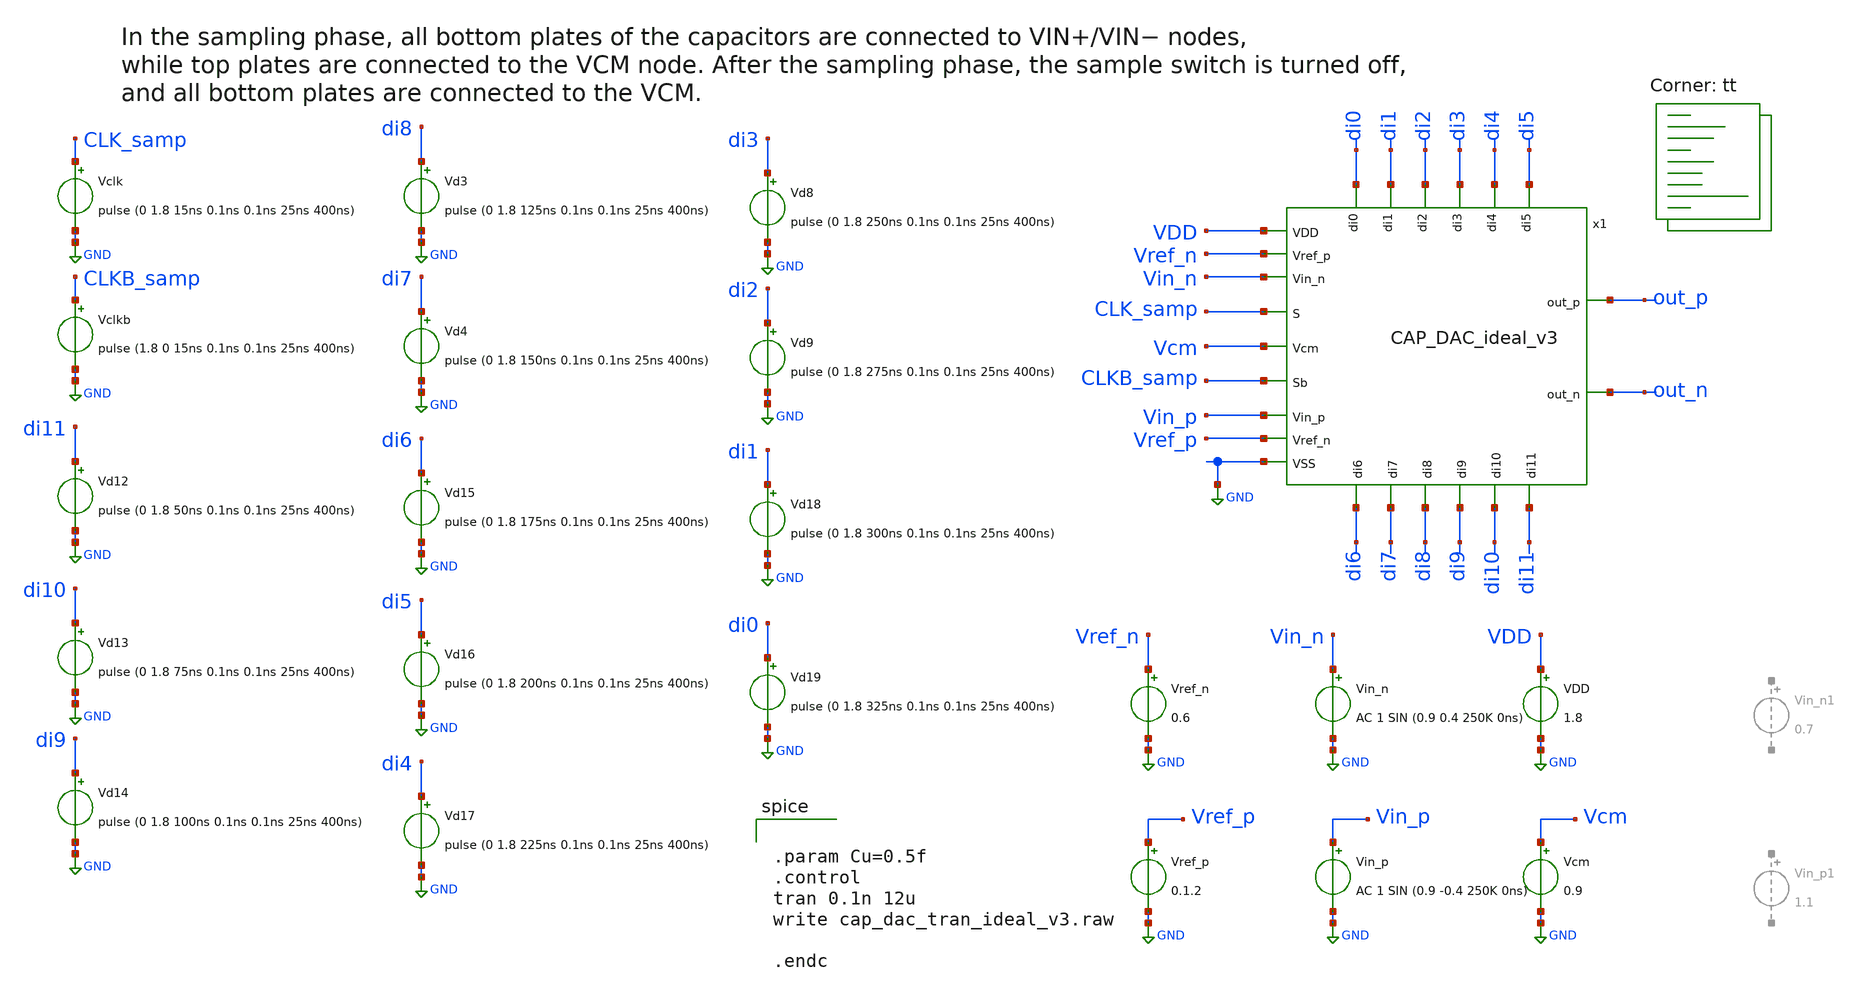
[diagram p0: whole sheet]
** sch_path: CAP_DAC_ideal_tb_v3.sch
**.subckt CAP_DAC_ideal_tb_v3
VDD VDD GND 1.8
Vclk CLK_samp GND pulse (0 1.8 15ns 0.1ns 0.1ns 25ns 400ns)
Vclkb CLKB_samp GND pulse (1.8 0 15ns 0.1ns 0.1ns 25ns 400ns)
Vcm Vcm GND 0.9
Vin_n Vin_n GND AC 1 SIN (0.9 0.4 250K 0ns)
Vin_p Vin_p GND AC 1 SIN (0.9 -0.4 250K 0ns)
Vref_n Vref_n GND 0.6
Vref_p Vref_p GND 0.1.2
x1 Vref_n Vin_n di0 di1 di2 VDD di3 GND di4 out_p Vcm di5 CLK_samp di6 CLKB_samp di7 out_n di8 di9
+ di10 di11 Vin_p Vref_p CAP_DAC_ideal_v3
Vd12 di11 GND pulse (0 1.8 50ns 0.1ns 0.1ns 25ns 400ns)
Vd13 di10 GND pulse (0 1.8 75ns 0.1ns 0.1ns 25ns 400ns)
Vd14 di9 GND pulse (0 1.8 100ns 0.1ns 0.1ns 25ns 400ns)
Vd15 di6 GND pulse (0 1.8 175ns 0.1ns 0.1ns 25ns 400ns)
Vd16 di5 GND pulse (0 1.8 200ns 0.1ns 0.1ns 25ns 400ns)
Vd17 di4 GND pulse (0 1.8 225ns 0.1ns 0.1ns 25ns 400ns)
Vd18 di1 GND pulse (0 1.8 300ns 0.1ns 0.1ns 25ns 400ns)
Vd19 di0 GND pulse (0 1.8 325ns 0.1ns 0.1ns 25ns 400ns)
Vd3 di8 GND pulse (0 1.8 125ns 0.1ns 0.1ns 25ns 400ns)
Vd4 di7 GND pulse (0 1.8 150ns 0.1ns 0.1ns 25ns 400ns)
Vd8 di3 GND pulse (0 1.8 250ns 0.1ns 0.1ns 25ns 400ns)
Vd9 di2 GND pulse (0 1.8 275ns 0.1ns 0.1ns 25ns 400ns)
**** begin user architecture code
.lib $::SKYWATER_MODELS/sky130.lib.spice tt


.param Cu=0.5f
.control
tran 0.1n 12u
write cap_dac_tran_ideal_v3.raw

.endc


**** end user architecture code
**.ends

* expanding   symbol:  project/CAP_DAC_ideal_v3.sym # of pins=23
** sym_path: CAP_DAC_ideal_v3.sym
** sch_path: CAP_DAC_ideal_v3.sch
.subckt CAP_DAC_ideal_v3 Vref_p Vin_n di0 di1 di2 VDD di3 VSS di4 out_p Vcm di5 S di6 Sb di7 out_n
+ di8 di9 di10 di11 Vin_p Vref_n
*.ipin VDD
*.ipin VSS
*.ipin S
*.ipin Sb
*.ipin di3
*.ipin Vcm
*.opin out_p
*.opin out_n
*.ipin Vref_p
*.ipin Vref_n
*.ipin di0
*.ipin di1
*.ipin di2
*.ipin di5
*.ipin di4
*.ipin di7
*.ipin di6
*.ipin di9
*.ipin di8
*.ipin di11
*.ipin di10
*.ipin Vin_n
*.ipin Vin_p
x30 VDD Vref_n Vref_p VSS S Sb d11 db11 in_p_sampled Vc1p Network_Switch
x31 VDD Vref_n Vref_p VSS S Sb d10 db10 in_p_sampled Vc2p Network_Switch
x32 VDD Vref_n Vref_p VSS S Sb d9 db9 in_p_sampled net11 Network_Switch
x33 VDD Vref_n Vref_p VSS S Sb d8 db8 in_p_sampled net12 Network_Switch
x34 VDD Vref_n Vref_p VSS S Sb d7 db7 in_p_sampled net13 Network_Switch
x35 VDD Vref_n Vref_p VSS S Sb d6 db6 in_p_sampled net14 Network_Switch
x36 VDD Vref_n Vref_p VSS S Sb d5 db5 in_p_sampled net15 Network_Switch
x37 VDD Vref_n Vref_p VSS S Sb d4 db4 in_p_sampled net16 Network_Switch
x38 VDD Vref_n Vref_p VSS S Sb d3 db3 in_p_sampled net17 Network_Switch
x39 VDD Vref_n Vref_p VSS S Sb d2 db2 in_p_sampled net18 Network_Switch
x40 VDD Vref_n Vref_p VSS S Sb d1 db1 in_p_sampled net19 Network_Switch
x41 VDD Vref_n Vref_p VSS S Sb d0 db0 in_p_sampled net20 Network_Switch
x42 VDD Vref_p Vref_n VSS S Sb d11 db11 in_n_sampled Vc1n Network_Switch
x43 VDD Vref_p Vref_n VSS S Sb d10 db10 in_n_sampled Vc2n Network_Switch
x44 VDD Vref_p Vref_n VSS S Sb d9 db9 in_n_sampled net10 Network_Switch
x45 VDD Vref_p Vref_n VSS S Sb d8 db8 in_n_sampled net9 Network_Switch
x46 VDD Vref_p Vref_n VSS S Sb d7 db7 in_n_sampled net8 Network_Switch
x47 VDD Vref_p Vref_n VSS S Sb d6 db6 in_n_sampled net7 Network_Switch
x48 VDD Vref_p Vref_n VSS S Sb d5 db5 in_n_sampled net6 Network_Switch
x49 VDD Vref_p Vref_n VSS S Sb d4 db4 in_n_sampled net5 Network_Switch
x50 VDD Vref_p Vref_n VSS S Sb d3 db3 in_n_sampled net4 Network_Switch
x51 VDD Vref_p Vref_n VSS S Sb d2 db2 in_n_sampled net3 Network_Switch
x52 VDD Vref_p Vref_n VSS S Sb d1 db1 in_n_sampled net2 Network_Switch
x53 VDD Vref_p Vref_n VSS S Sb d0 db0 in_n_sampled net1 Network_Switch
x27 out_n Sb S VDD VSS out_p transmission_gate
x2 VDD di0 db0 VSS Inverter
x3 VDD db0 d0 VSS Inverter
x4 VDD di1 db1 VSS Inverter
x5 VDD db1 d1 VSS Inverter
x6 VDD di2 db2 VSS Inverter
x7 VDD db2 d2 VSS Inverter
x8 VDD di3 db3 VSS Inverter
x9 VDD db3 d3 VSS Inverter
x10 VDD di4 db4 VSS Inverter
x11 VDD db4 d4 VSS Inverter
x12 VDD di5 db5 VSS Inverter
x13 VDD db5 d5 VSS Inverter
x14 VDD di6 db6 VSS Inverter
x15 VDD db6 d6 VSS Inverter
x16 VDD di7 db7 VSS Inverter
x17 VDD db7 d7 VSS Inverter
x18 VDD di8 db8 VSS Inverter
x19 VDD db8 d8 VSS Inverter
x20 VDD di9 db9 VSS Inverter
x21 VDD db9 d9 VSS Inverter
x22 VDD di10 db10 VSS Inverter
x23 VDD db10 d10 VSS Inverter
x24 VDD di11 db11 VSS Inverter
x25 VDD db11 d11 VSS Inverter
x28 Vcm Sb S VDD VSS out_p transmission_gate
x29 Vcm Sb S VDD VSS out_n transmission_gate
x1 VDD Vref_p Vref_n VSS S Sb VSS VDD in_n_sampled noden Network_Switch
x26 VDD Vref_n Vref_p VSS S Sb VSS VDD in_p_sampled nodep Network_Switch
x54 VDD Vin_n Sb S in_n_sampled VSS bootstrapped_switch
x55 VDD Vin_p Sb S in_p_sampled VSS bootstrapped_switch
C27 out_n net20 {Cu} m=1
C28 out_n net19 {2*Cu} m=1
C29 out_n net18 {4*Cu} m=1
C30 out_n net17 {8*Cu} m=1
C31 out_n net16 {16*Cu} m=1
C32 out_n net15 {32*Cu} m=1
C33 out_n net14 {64*Cu} m=1
C34 out_n net13 {128*Cu} m=1
C35 out_n net12 {256*Cu} m=1
C36 out_n net11 {512*Cu} m=1
C37 out_n Vc2p {1024*Cu} m=1
C38 out_n Vc1p {2048*Cu} m=1
C39 out_n nodep {Cu} m=1
C40 net1 out_p {Cu} m=1
C41 net2 out_p {2*Cu} m=1
C42 net3 out_p {4*Cu} m=1
C43 net4 out_p {8*Cu} m=1
C44 net5 out_p {16*Cu} m=1
C45 net6 out_p {32*Cu} m=1
C46 net7 out_p {64*Cu} m=1
C47 net8 out_p {128*Cu} m=1
C48 net9 out_p {256*Cu} m=1
C49 net10 out_p {512*Cu} m=1
C50 Vc2n out_p {1024*Cu} m=1
C51 Vc1n out_p {2048*Cu} m=1
C52 noden out_p {Cu} m=1
.ends


* expanding   symbol:  Network_Switch.sym # of pins=10
** sym_path: Network_Switch.sym
** sch_path: Network_Switch.sch
.subckt Network_Switch VDD ground Vref VSS S Sb d db Vin Vout
*.ipin ground
*.ipin Vref
*.ipin Vin
*.opin Vout
*.ipin VDD
*.ipin VSS
*.ipin S
*.ipin Sb
*.ipin d
*.ipin db
x1 ground d db VDD VSS net1 transmission_gate
x2 Vref db d VDD VSS net1 transmission_gate
x3 net1 S Sb VDD VSS Vout transmission_gate
x4 Vin Sb S VDD VSS Vout transmission_gate
.ends


* expanding   symbol:  transmission_gate.sym # of pins=6
** sym_path: transmission_gate.sym
** sch_path: transmission_gate.sch
.subckt transmission_gate in clkb clk VDD VSS out
*.ipin in
*.ipin clk
*.ipin clkb
*.opin out
*.ipin VDD
*.ipin VSS
XM1 out clk in VSS sky130_fd_pr__nfet_01v8 L=0.15 W=0.5 nf=1 ad='int((nf+1)/2) * W/nf * 0.29' as='int((nf+2)/2) * W/nf * 0.29'
+ pd='2*int((nf+1)/2) * (W/nf + 0.29)' ps='2*int((nf+2)/2) * (W/nf + 0.29)' nrd='0.29 / W' nrs='0.29 / W'
+ sa=0 sb=0 sd=0 mult=1 m=1
XM2 out clkb in VDD sky130_fd_pr__pfet_01v8 L=0.15 W=0.5 nf=1 ad='int((nf+1)/2) * W/nf * 0.29' as='int((nf+2)/2) * W/nf * 0.29'
+ pd='2*int((nf+1)/2) * (W/nf + 0.29)' ps='2*int((nf+2)/2) * (W/nf + 0.29)' nrd='0.29 / W' nrs='0.29 / W'
+ sa=0 sb=0 sd=0 mult=1 m=1
.ends


* expanding   symbol:  Inverter.sym # of pins=4
** sym_path: Inverter.sym
** sch_path: Inverter.sch
.subckt Inverter VDD IN OUT VSS
*.ipin IN
*.ipin VSS
*.ipin VDD
*.opin OUT
XM1 OUT IN VSS VSS sky130_fd_pr__nfet_01v8 L=0.3 W=1 nf=1 ad='int((nf+1)/2) * W/nf * 0.29' as='int((nf+2)/2) * W/nf * 0.29'
+ pd='2*int((nf+1)/2) * (W/nf + 0.29)' ps='2*int((nf+2)/2) * (W/nf + 0.29)' nrd='0.29 / W' nrs='0.29 / W'
+ sa=0 sb=0 sd=0 mult=1 m=1
XM2 OUT IN VDD VDD sky130_fd_pr__pfet_01v8 L=0.3 W=2 nf=1 ad='int((nf+1)/2) * W/nf * 0.29' as='int((nf+2)/2) * W/nf * 0.29'
+ pd='2*int((nf+1)/2) * (W/nf + 0.29)' ps='2*int((nf+2)/2) * (W/nf + 0.29)' nrd='0.29 / W' nrs='0.29 / W'
+ sa=0 sb=0 sd=0 mult=1 m=1
.ends


* expanding   symbol:  bootstrapped_switch.sym # of pins=6
** sym_path: bootstrapped_switch.sym
** sch_path: bootstrapped_switch.sch
.subckt bootstrapped_switch VDD in clkb clk out VSS
*.ipin in
*.opin out
*.ipin VSS
*.ipin VDD
*.ipin clkb
*.ipin clk
XM1 net4 clkb net5 net5 sky130_fd_pr__nfet_01v8 L=0.15 W=2 nf=1 ad='int((nf+1)/2) * W/nf * 0.29' as='int((nf+2)/2) * W/nf * 0.29'
+ pd='2*int((nf+1)/2) * (W/nf + 0.29)' ps='2*int((nf+2)/2) * (W/nf + 0.29)' nrd='0.29 / W' nrs='0.29 / W'
+ sa=0 sb=0 sd=0 mult=1 m=1
XM2 in Vg net4 VSS sky130_fd_pr__nfet_01v8 L=1 W=0.5 nf=1 ad='int((nf+1)/2) * W/nf * 0.29' as='int((nf+2)/2) * W/nf * 0.29'
+ pd='2*int((nf+1)/2) * (W/nf + 0.29)' ps='2*int((nf+2)/2) * (W/nf + 0.29)' nrd='0.29 / W' nrs='0.29 / W'
+ sa=0 sb=0 sd=0 mult=1 m=1
XM3 Vp Vg net1 Vp sky130_fd_pr__pfet_01v8 L=0.15 W=2 nf=1 ad='int((nf+1)/2) * W/nf * 0.29' as='int((nf+2)/2) * W/nf * 0.29'
+ pd='2*int((nf+1)/2) * (W/nf + 0.29)' ps='2*int((nf+2)/2) * (W/nf + 0.29)' nrd='0.29 / W' nrs='0.29 / W'
+ sa=0 sb=0 sd=0 mult=1 m=1
XM5 out Vg in VSS sky130_fd_pr__nfet_01v8 L=0.15 W=30 nf=1 ad='int((nf+1)/2) * W/nf * 0.29' as='int((nf+2)/2) * W/nf * 0.29'
+ pd='2*int((nf+1)/2) * (W/nf + 0.29)' ps='2*int((nf+2)/2) * (W/nf + 0.29)' nrd='0.29 / W' nrs='0.29 / W'
+ sa=0 sb=0 sd=0 mult=1 m=1
XM6 out clkb in VDD sky130_fd_pr__pfet_01v8 L=0.15 W=30 nf=1 ad='int((nf+1)/2) * W/nf * 0.29' as='int((nf+2)/2) * W/nf * 0.29'
+ pd='2*int((nf+1)/2) * (W/nf + 0.29)' ps='2*int((nf+2)/2) * (W/nf + 0.29)' nrd='0.29 / W' nrs='0.29 / W'
+ sa=0 sb=0 sd=0 mult=1 m=1
XM8 net6 clkb net2 net2 sky130_fd_pr__nfet_01v8 L=0.15 W=0.5 nf=1 ad='int((nf+1)/2) * W/nf * 0.29' as='int((nf+2)/2) * W/nf * 0.29'
+ pd='2*int((nf+1)/2) * (W/nf + 0.29)' ps='2*int((nf+2)/2) * (W/nf + 0.29)' nrd='0.29 / W' nrs='0.29 / W'
+ sa=0 sb=0 sd=0 mult=1 m=1
XC1 net4 Vp sky130_fd_pr__cap_mim_m3_1 W=18 L=18 MF=10 m=10
XM7 Vg VDD net6 net6 sky130_fd_pr__nfet_01v8 L=0.15 W=0.5 nf=1 ad='int((nf+1)/2) * W/nf * 0.29' as='int((nf+2)/2) * W/nf * 0.29'
+ pd='2*int((nf+1)/2) * (W/nf + 0.29)' ps='2*int((nf+2)/2) * (W/nf + 0.29)' nrd='0.29 / W' nrs='0.29 / W'
+ sa=0 sb=0 sd=0 mult=1 m=1
XM4 Vg net3 Vp Vp sky130_fd_pr__pfet_01v8 L=0.15 W=0.5 nf=1 ad='int((nf+1)/2) * W/nf * 0.29' as='int((nf+2)/2) * W/nf * 0.29'
+ pd='2*int((nf+1)/2) * (W/nf + 0.29)' ps='2*int((nf+2)/2) * (W/nf + 0.29)' nrd='0.29 / W' nrs='0.29 / W'
+ sa=0 sb=0 sd=0 mult=1 m=1
XC2 out VSS sky130_fd_pr__cap_mim_m3_1 W=36 L=36 MF=20 m=20
XM10 net1 clk net7 net1 sky130_fd_pr__pfet_01v8 L=0.15 W=2 nf=1 ad='int((nf+1)/2) * W/nf * 0.29' as='int((nf+2)/2) * W/nf * 0.29'
+ pd='2*int((nf+1)/2) * (W/nf + 0.29)' ps='2*int((nf+2)/2) * (W/nf + 0.29)' nrd='0.29 / W' nrs='0.29 / W'
+ sa=0 sb=0 sd=0 mult=1 m=1
XM11 net5 clkb net8 net8 sky130_fd_pr__nfet_01v8 L=0.15 W=2 nf=1 ad='int((nf+1)/2) * W/nf * 0.29' as='int((nf+2)/2) * W/nf * 0.29'
+ pd='2*int((nf+1)/2) * (W/nf + 0.29)' ps='2*int((nf+2)/2) * (W/nf + 0.29)' nrd='0.29 / W' nrs='0.29 / W'
+ sa=0 sb=0 sd=0 mult=1 m=1
XM12 net7 clk VDD net7 sky130_fd_pr__pfet_01v8 L=0.15 W=2 nf=1 ad='int((nf+1)/2) * W/nf * 0.29' as='int((nf+2)/2) * W/nf * 0.29'
+ pd='2*int((nf+1)/2) * (W/nf + 0.29)' ps='2*int((nf+2)/2) * (W/nf + 0.29)' nrd='0.29 / W' nrs='0.29 / W'
+ sa=0 sb=0 sd=0 mult=1 m=1
XM13 net8 clkb VSS VSS sky130_fd_pr__nfet_01v8 L=0.15 W=2 nf=1 ad='int((nf+1)/2) * W/nf * 0.29' as='int((nf+2)/2) * W/nf * 0.29'
+ pd='2*int((nf+1)/2) * (W/nf + 0.29)' ps='2*int((nf+2)/2) * (W/nf + 0.29)' nrd='0.29 / W' nrs='0.29 / W'
+ sa=0 sb=0 sd=0 mult=1 m=1
XM14 net2 clkb VSS VSS sky130_fd_pr__nfet_01v8 L=0.15 W=0.5 nf=1 ad='int((nf+1)/2) * W/nf * 0.29' as='int((nf+2)/2) * W/nf * 0.29'
+ pd='2*int((nf+1)/2) * (W/nf + 0.29)' ps='2*int((nf+2)/2) * (W/nf + 0.29)' nrd='0.29 / W' nrs='0.29 / W'
+ sa=0 sb=0 sd=0 mult=1 m=1
XM15 net3 clk VDD VDD sky130_fd_pr__pfet_01v8 L=0.15 W=1 nf=1 ad='int((nf+1)/2) * W/nf * 0.29' as='int((nf+2)/2) * W/nf * 0.29'
+ pd='2*int((nf+1)/2) * (W/nf + 0.29)' ps='2*int((nf+2)/2) * (W/nf + 0.29)' nrd='0.29 / W' nrs='0.29 / W'
+ sa=0 sb=0 sd=0 mult=1 m=1
XM16 net3 clk net4 VSS sky130_fd_pr__nfet_01v8 L=1 W=0.5 nf=1 ad='int((nf+1)/2) * W/nf * 0.29' as='int((nf+2)/2) * W/nf * 0.29'
+ pd='2*int((nf+1)/2) * (W/nf + 0.29)' ps='2*int((nf+2)/2) * (W/nf + 0.29)' nrd='0.29 / W' nrs='0.29 / W'
+ sa=0 sb=0 sd=0 mult=1 m=1
XM17 net3 Vg net4 VSS sky130_fd_pr__nfet_01v8 L=0.15 W=2 nf=1 ad='int((nf+1)/2) * W/nf * 0.29' as='int((nf+2)/2) * W/nf * 0.29'
+ pd='2*int((nf+1)/2) * (W/nf + 0.29)' ps='2*int((nf+2)/2) * (W/nf + 0.29)' nrd='0.29 / W' nrs='0.29 / W'
+ sa=0 sb=0 sd=0 mult=1 m=1
.ends

.GLOBAL GND
.end
